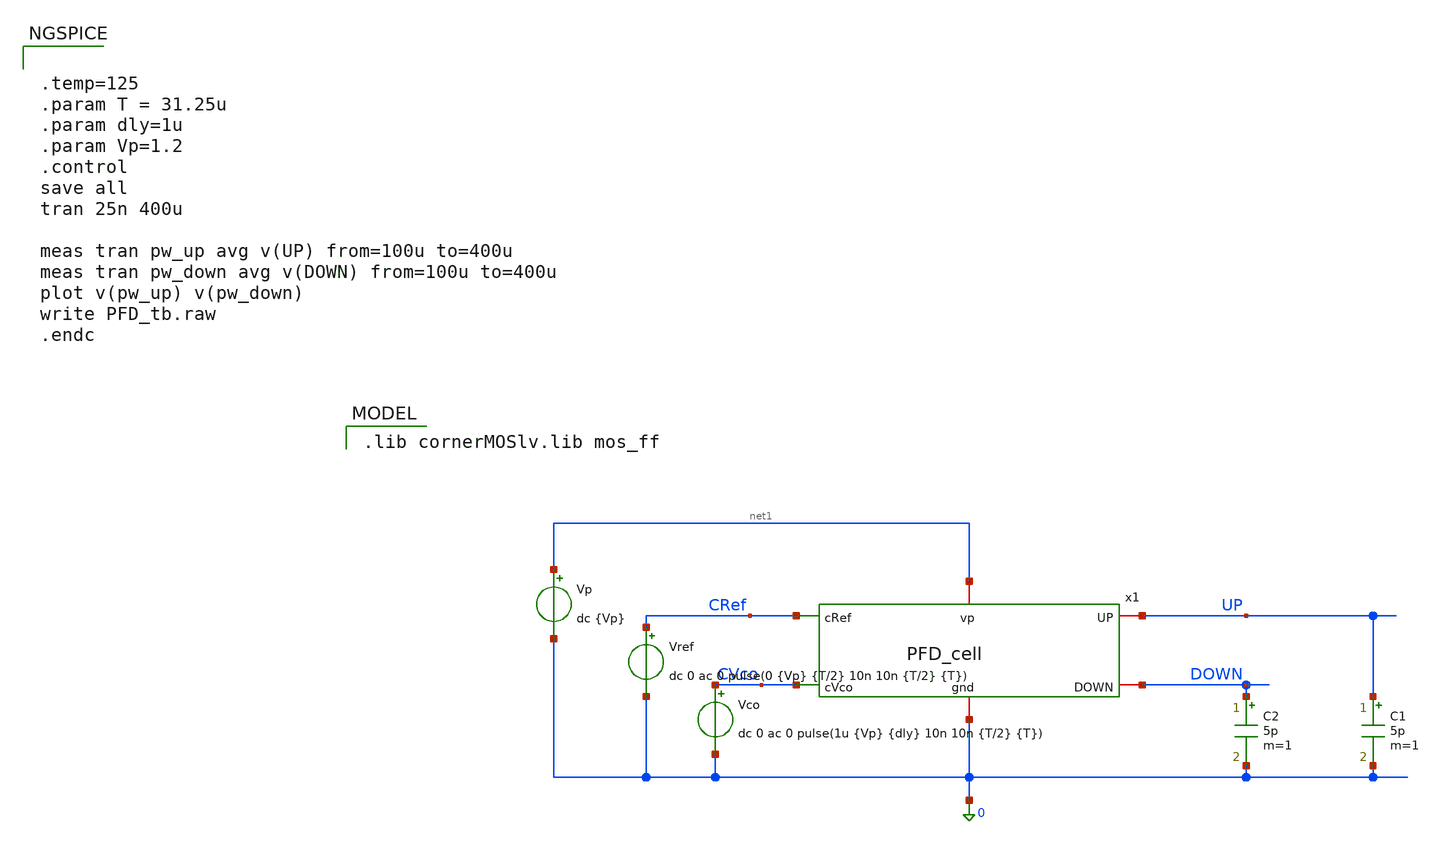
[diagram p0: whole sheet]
** sch_path: PFD/PFD_tb.sch
**.subckt PFD_tb
Vref CRef 0 dc 0 ac 0 pulse(0 {Vp} {T/2} 10n 10n {T/2} {T})
Vco CVco 0 dc 0 ac 0 pulse(1u {Vp} {dly} 10n 10n {T/2} {T})
Vp net1 0 dc {Vp}
C1 UP 0 5p m=1
C2 DOWN 0 5p m=1
x1 0 net1 CRef UP DOWN CVco PFD_cell
**** begin user architecture code
 .lib cornerMOSlv.lib mos_ff



.temp=125
.param T = 31.25u
.param dly=1u
.param Vp=1.2
.control
save all
tran 25n 400u

meas tran pw_up avg v(UP) from=100u to=400u
meas tran pw_down avg v(DOWN) from=100u to=400u
plot v(pw_up) v(pw_down)
write PFD_tb.raw
.endc


**** end user architecture code
**.ends
.end
